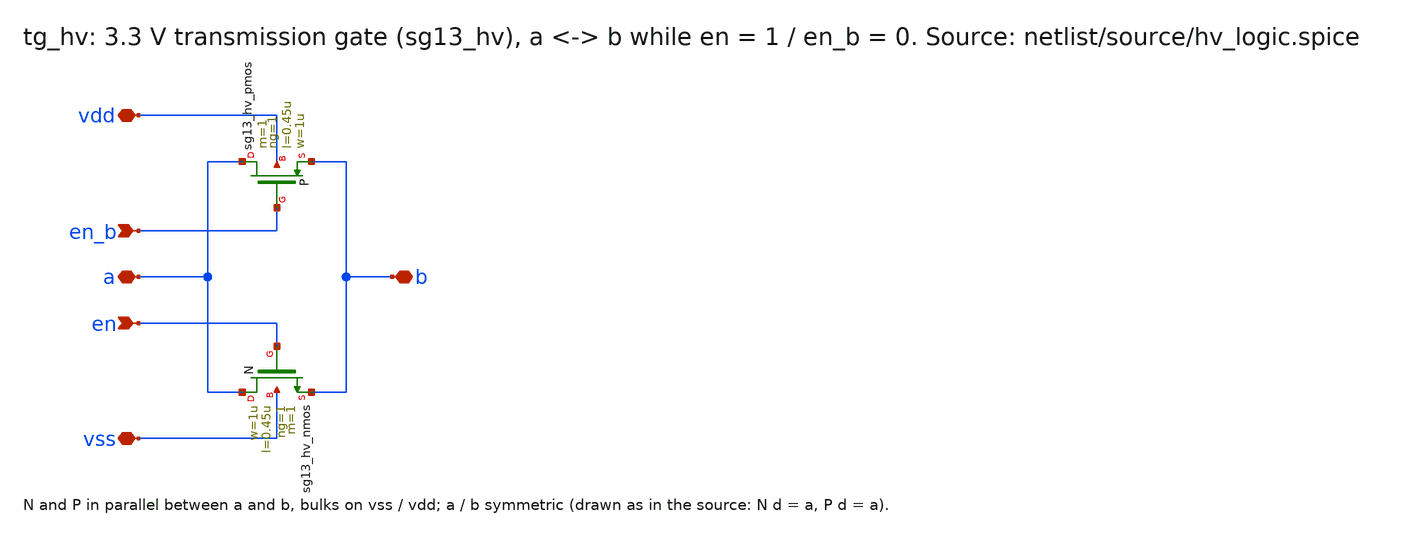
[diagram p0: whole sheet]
** sch_path: macros/hv_logic/schematic/xschem/tg_hv.sch
**.subckt tg_hv vdd vss en en_b a b
*.iopin vdd
*.iopin vss
*.ipin en
*.ipin en_b
*.iopin a
*.iopin b
XN a en b vss sg13_hv_nmos w=1u l=0.45u ng=1 m=1 mm_ok=1
XP a en_b b vdd sg13_hv_pmos w=1u l=0.45u ng=1 m=1 mm_ok=1
**.ends
.end
